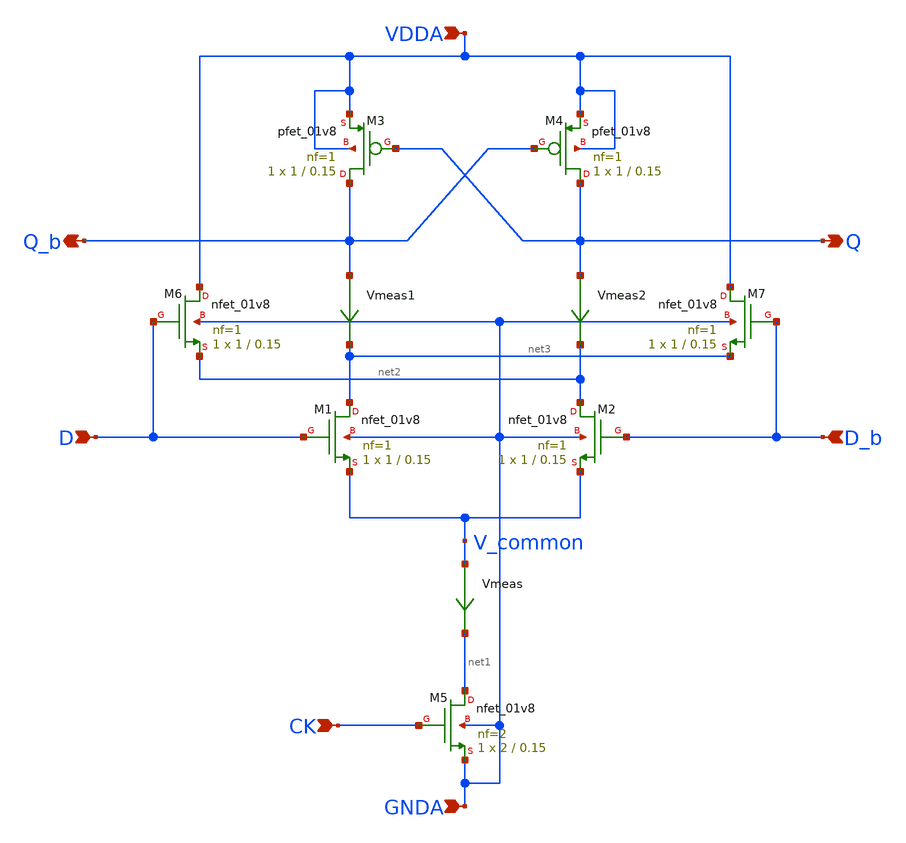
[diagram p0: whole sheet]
** sch_path: projects/pll/divider/xschem_ngspice/xcp_latch_SF.sch
**.subckt xcp_latch_SF D Q D_b CK Q_b VDDA GNDA
*.ipin D
*.opin Q
*.ipin D_b
*.ipin CK
*.opin Q_b
*.ipin VDDA
*.ipin GNDA
XM5 net1 CK GNDA GNDA sky130_fd_pr__nfet_01v8 L=0.15 W=2 nf=2 ad='int((nf+1)/2) * W/nf * 0.29' as='int((nf+2)/2) * W/nf * 0.29'
+ pd='2*int((nf+1)/2) * (W/nf + 0.29)' ps='2*int((nf+2)/2) * (W/nf + 0.29)' nrd='0.29 / W' nrs='0.29 / W'
+ sa=0 sb=0 sd=0 mult=1 m=1
XM1 net3 D V_common GNDA sky130_fd_pr__nfet_01v8 L=0.15 W=1 nf=1 ad='int((nf+1)/2) * W/nf * 0.29' as='int((nf+2)/2) * W/nf * 0.29'
+ pd='2*int((nf+1)/2) * (W/nf + 0.29)' ps='2*int((nf+2)/2) * (W/nf + 0.29)' nrd='0.29 / W' nrs='0.29 / W'
+ sa=0 sb=0 sd=0 mult=1 m=1
XM2 net2 D_b V_common GNDA sky130_fd_pr__nfet_01v8 L=0.15 W=1 nf=1 ad='int((nf+1)/2) * W/nf * 0.29' as='int((nf+2)/2) * W/nf * 0.29'
+ pd='2*int((nf+1)/2) * (W/nf + 0.29)' ps='2*int((nf+2)/2) * (W/nf + 0.29)' nrd='0.29 / W' nrs='0.29 / W'
+ sa=0 sb=0 sd=0 mult=1 m=1
Vmeas V_common net1 0
.save i(vmeas)
Vmeas1 Q_b net3 0
.save i(vmeas1)
Vmeas2 Q net2 0
.save i(vmeas2)
XM3 Q_b Q VDDA VDDA sky130_fd_pr__pfet_01v8 L=0.15 W=1 nf=1 ad='int((nf+1)/2) * W/nf * 0.29' as='int((nf+2)/2) * W/nf * 0.29'
+ pd='2*int((nf+1)/2) * (W/nf + 0.29)' ps='2*int((nf+2)/2) * (W/nf + 0.29)' nrd='0.29 / W' nrs='0.29 / W'
+ sa=0 sb=0 sd=0 mult=1 m=1
XM4 Q Q_b VDDA VDDA sky130_fd_pr__pfet_01v8 L=0.15 W=1 nf=1 ad='int((nf+1)/2) * W/nf * 0.29' as='int((nf+2)/2) * W/nf * 0.29'
+ pd='2*int((nf+1)/2) * (W/nf + 0.29)' ps='2*int((nf+2)/2) * (W/nf + 0.29)' nrd='0.29 / W' nrs='0.29 / W'
+ sa=0 sb=0 sd=0 mult=1 m=1
XM6 VDDA D net2 GNDA sky130_fd_pr__nfet_01v8 L=0.15 W=1 nf=1 ad='int((nf+1)/2) * W/nf * 0.29' as='int((nf+2)/2) * W/nf * 0.29'
+ pd='2*int((nf+1)/2) * (W/nf + 0.29)' ps='2*int((nf+2)/2) * (W/nf + 0.29)' nrd='0.29 / W' nrs='0.29 / W'
+ sa=0 sb=0 sd=0 mult=1 m=1
XM7 VDDA D_b net3 GNDA sky130_fd_pr__nfet_01v8 L=0.15 W=1 nf=1 ad='int((nf+1)/2) * W/nf * 0.29' as='int((nf+2)/2) * W/nf * 0.29'
+ pd='2*int((nf+1)/2) * (W/nf + 0.29)' ps='2*int((nf+2)/2) * (W/nf + 0.29)' nrd='0.29 / W' nrs='0.29 / W'
+ sa=0 sb=0 sd=0 mult=1 m=1
**.ends
.end
